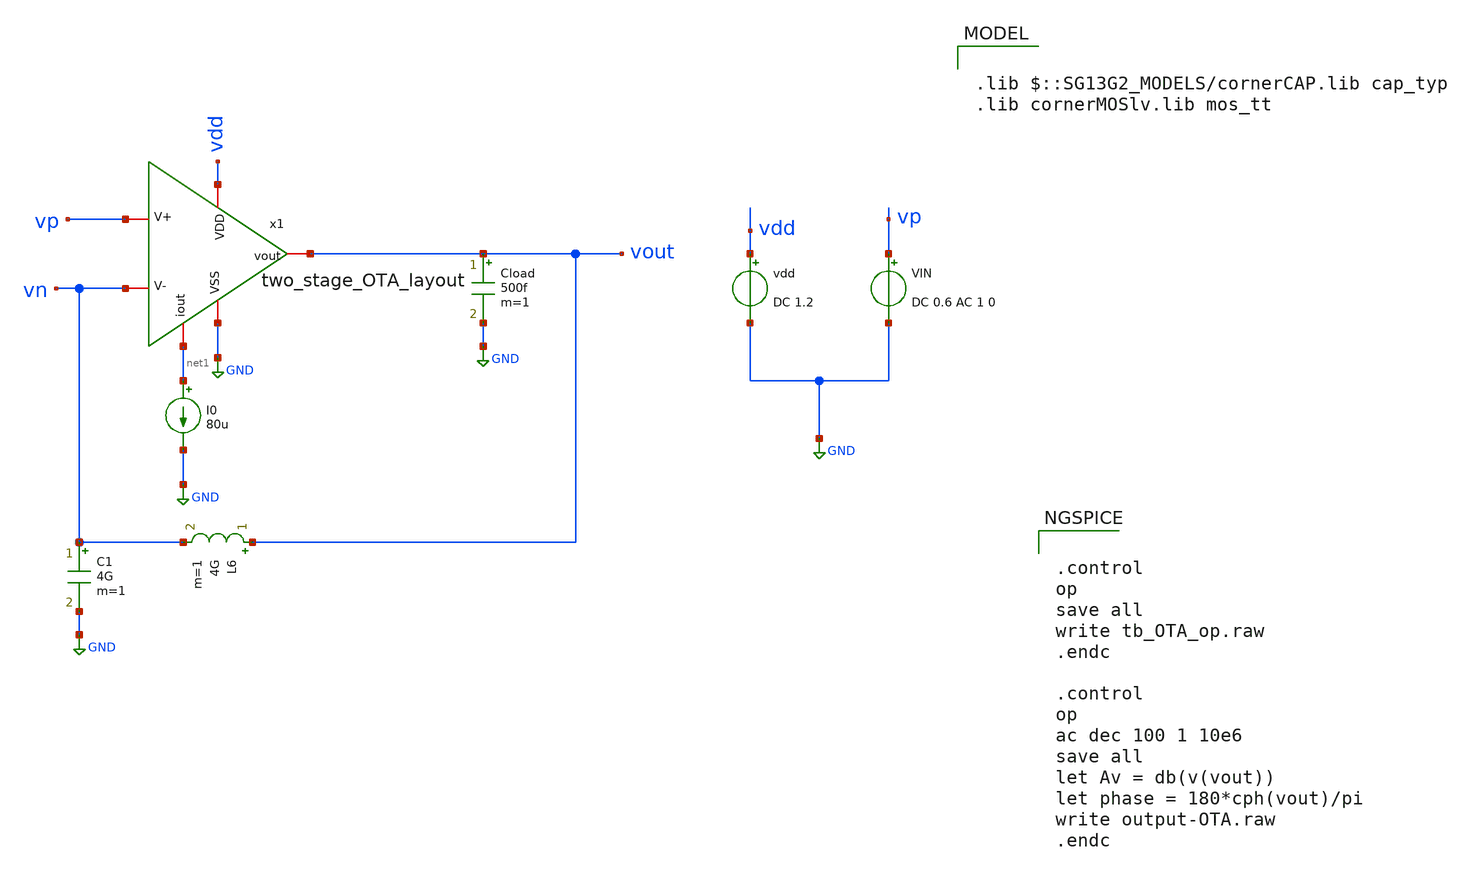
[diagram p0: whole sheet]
** sch_path: BTDay7-Ex/Test-OTA.sch
**.subckt Test-OTA
I0 net1 GND 80u
Cload vout GND 500f m=1
vdd vdd GND DC 1.2
VIN vp GND DC 0.6 AC 1 0
C1 vn GND 4G m=1
L6 vout vn 4G m=1
x1 vn vp GND vdd net1 vout two_stage_OTA_layout
**** begin user architecture code

.lib $::SG13G2_MODELS/cornerCAP.lib cap_typ
.lib cornerMOSlv.lib mos_tt



.control
op
save all
write tb_OTA_op.raw
.endc

.control
op
ac dec 100 1 10e6
save all
let Av = db(v(vout))
let phase = 180*cph(vout)/pi
write output-OTA.raw
.endc


**** end user architecture code
**.ends
.GLOBAL GND
.end
